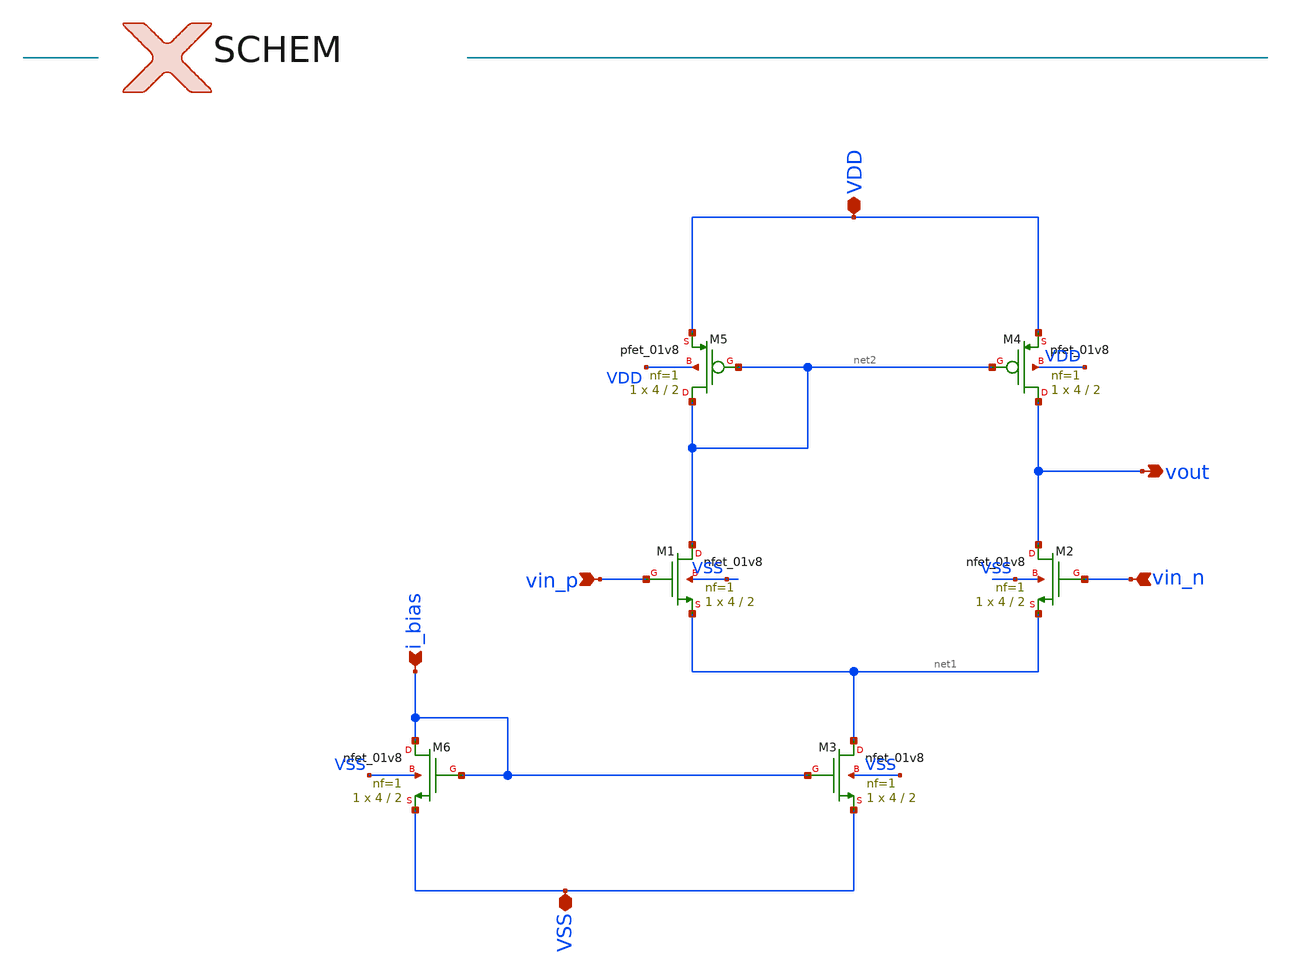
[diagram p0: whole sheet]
** sch_path: ISSCC_2025_V1/xschem/Benchmark_Circuits/OpAmp/OpAmp.sch
**.subckt OpAmp vin_p vin_n VSS VDD vout i_bias
*.ipin vin_p
*.ipin vin_n
*.iopin VSS
*.iopin VDD
*.opin vout
*.ipin i_bias
XM1 net2 vin_p net1 VSS sky130_fd_pr__nfet_01v8 L=2 W=4 nf=1 ad='int((nf+1)/2) * W/nf * 0.29' as='int((nf+2)/2) * W/nf * 0.29'
+ pd='2*int((nf+1)/2) * (W/nf + 0.29)' ps='2*int((nf+2)/2) * (W/nf + 0.29)' nrd='0.29 / W' nrs='0.29 / W'
+ sa=0 sb=0 sd=0 mult=1 m=1
XM2 vout vin_n net1 VSS sky130_fd_pr__nfet_01v8 L=2 W=4 nf=1 ad='int((nf+1)/2) * W/nf * 0.29' as='int((nf+2)/2) * W/nf * 0.29'
+ pd='2*int((nf+1)/2) * (W/nf + 0.29)' ps='2*int((nf+2)/2) * (W/nf + 0.29)' nrd='0.29 / W' nrs='0.29 / W'
+ sa=0 sb=0 sd=0 mult=1 m=1
XM3 net1 i_bias VSS VSS sky130_fd_pr__nfet_01v8 L=2 W=4 nf=1 ad='int((nf+1)/2) * W/nf * 0.29' as='int((nf+2)/2) * W/nf * 0.29'
+ pd='2*int((nf+1)/2) * (W/nf + 0.29)' ps='2*int((nf+2)/2) * (W/nf + 0.29)' nrd='0.29 / W' nrs='0.29 / W'
+ sa=0 sb=0 sd=0 mult=1 m=1
XM6 i_bias i_bias VSS VSS sky130_fd_pr__nfet_01v8 L=2 W=4 nf=1 ad='int((nf+1)/2) * W/nf * 0.29' as='int((nf+2)/2) * W/nf * 0.29'
+ pd='2*int((nf+1)/2) * (W/nf + 0.29)' ps='2*int((nf+2)/2) * (W/nf + 0.29)' nrd='0.29 / W' nrs='0.29 / W'
+ sa=0 sb=0 sd=0 mult=1 m=1
XM4 vout net2 VDD VDD sky130_fd_pr__pfet_01v8 L=2 W=4 nf=1 ad='int((nf+1)/2) * W/nf * 0.29' as='int((nf+2)/2) * W/nf * 0.29'
+ pd='2*int((nf+1)/2) * (W/nf + 0.29)' ps='2*int((nf+2)/2) * (W/nf + 0.29)' nrd='0.29 / W' nrs='0.29 / W'
+ sa=0 sb=0 sd=0 mult=1 m=1
XM5 net2 net2 VDD VDD sky130_fd_pr__pfet_01v8 L=2 W=4 nf=1 ad='int((nf+1)/2) * W/nf * 0.29' as='int((nf+2)/2) * W/nf * 0.29'
+ pd='2*int((nf+1)/2) * (W/nf + 0.29)' ps='2*int((nf+2)/2) * (W/nf + 0.29)' nrd='0.29 / W' nrs='0.29 / W'
+ sa=0 sb=0 sd=0 mult=1 m=1
**.ends
.end
